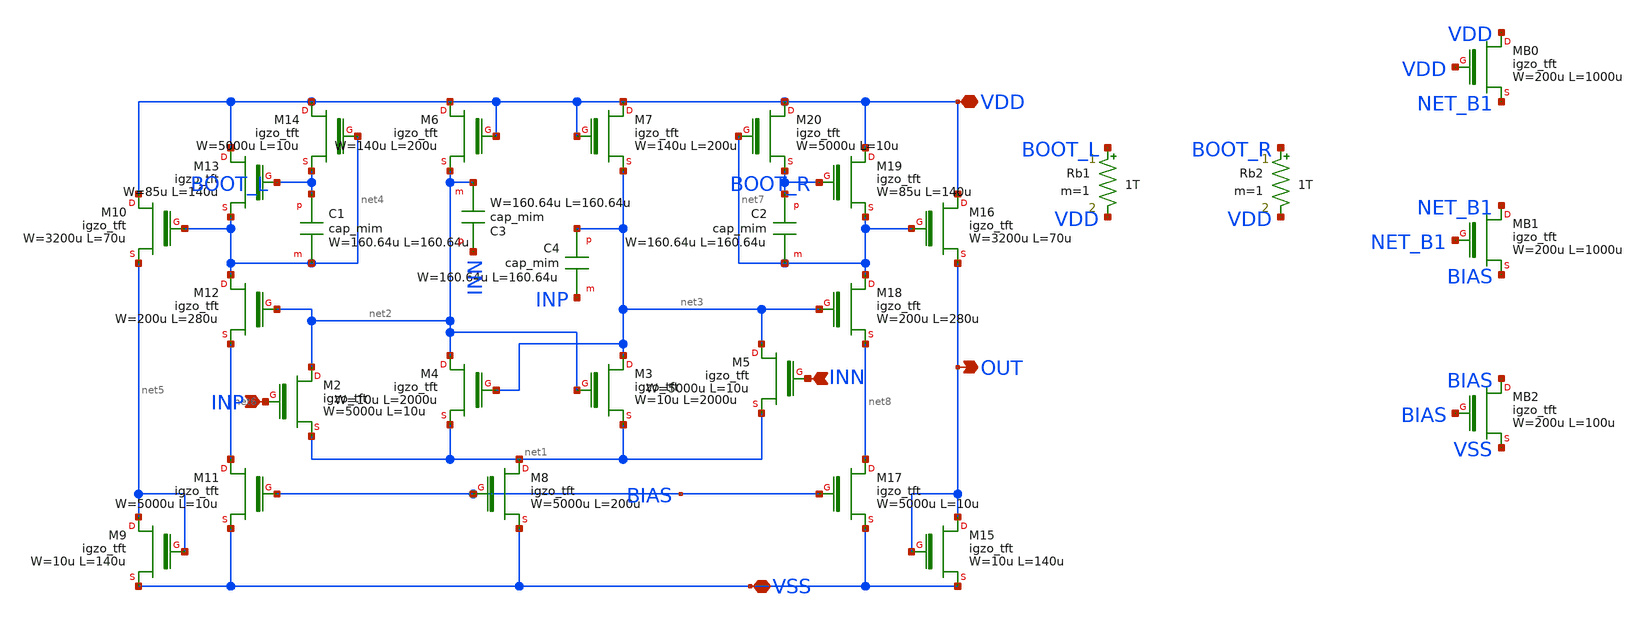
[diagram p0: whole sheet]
** sch_path: OPAM/OPAM_BIASED.sch
**.subckt OPAM_BIASED INP VDD INN VSS OUT
*.ipin INP
*.iopin VDD
*.ipin INN
*.iopin VSS
*.opin OUT
XM2 net2 INP net1 igzo_tft W=5000u L=10u ov=5u nf=1 m=1
XM4 net2 net3 net1 igzo_tft W=10u L=2000u ov=5u nf=1 m=1
XM3 net3 net2 net1 igzo_tft W=10u L=2000u ov=5u nf=1 m=1
XM5 net3 INN net1 igzo_tft W=5000u L=10u ov=5u nf=1 m=1
XM6 VDD VDD net2 igzo_tft W=140u L=200u ov=5u nf=1 m=1
XM7 VDD VDD net3 igzo_tft W=140u L=200u ov=5u nf=1 m=1
XM8 net1 BIAS VSS igzo_tft W=5000u L=200u ov=5u nf=1 m=1
XM9 net5 net5 VSS igzo_tft W=10u L=140u ov=5u nf=1 m=1
XM10 VDD net4 net5 igzo_tft W=3200u L=70u ov=5u nf=1 m=1
XM11 net6 BIAS VSS igzo_tft W=5000u L=10u ov=5u nf=1 m=1
XM12 net4 net2 net6 igzo_tft W=200u L=280u ov=5u nf=1 m=1
XM13 VDD BOOT_L net4 igzo_tft W=85u L=140u ov=5u nf=1 m=1
XM14 VDD net4 BOOT_L igzo_tft W=5000u L=10u ov=5u nf=1 m=1
XC1 BOOT_L net4 cap_mim W=160.64u L=160.64u
XM15 OUT OUT VSS igzo_tft W=10u L=140u ov=5u nf=1 m=1
XM16 VDD net7 OUT igzo_tft W=3200u L=70u ov=5u nf=1 m=1
XM17 net8 BIAS VSS igzo_tft W=5000u L=10u ov=5u nf=1 m=1
XM18 net7 net3 net8 igzo_tft W=200u L=280u ov=5u nf=1 m=1
XM19 VDD BOOT_R net7 igzo_tft W=85u L=140u ov=5u nf=1 m=1
XM20 VDD net7 BOOT_R igzo_tft W=5000u L=10u ov=5u nf=1 m=1
XC2 BOOT_R net7 cap_mim W=160.64u L=160.64u
XC3 INN net2 cap_mim W=160.64u L=160.64u
XC4 net3 INP cap_mim W=160.64u L=160.64u
Rb1 BOOT_L VDD 1T m=1
Rb2 BOOT_R VDD 1T m=1
XMB0 VDD VDD NET_B1 igzo_tft W=200u L=1000u ov=5u nf=1 m=1
XMB1 NET_B1 NET_B1 BIAS igzo_tft W=200u L=1000u ov=5u nf=1 m=1
XMB2 BIAS BIAS VSS igzo_tft W=200u L=100u ov=5u nf=1 m=1
**.ends
.end
